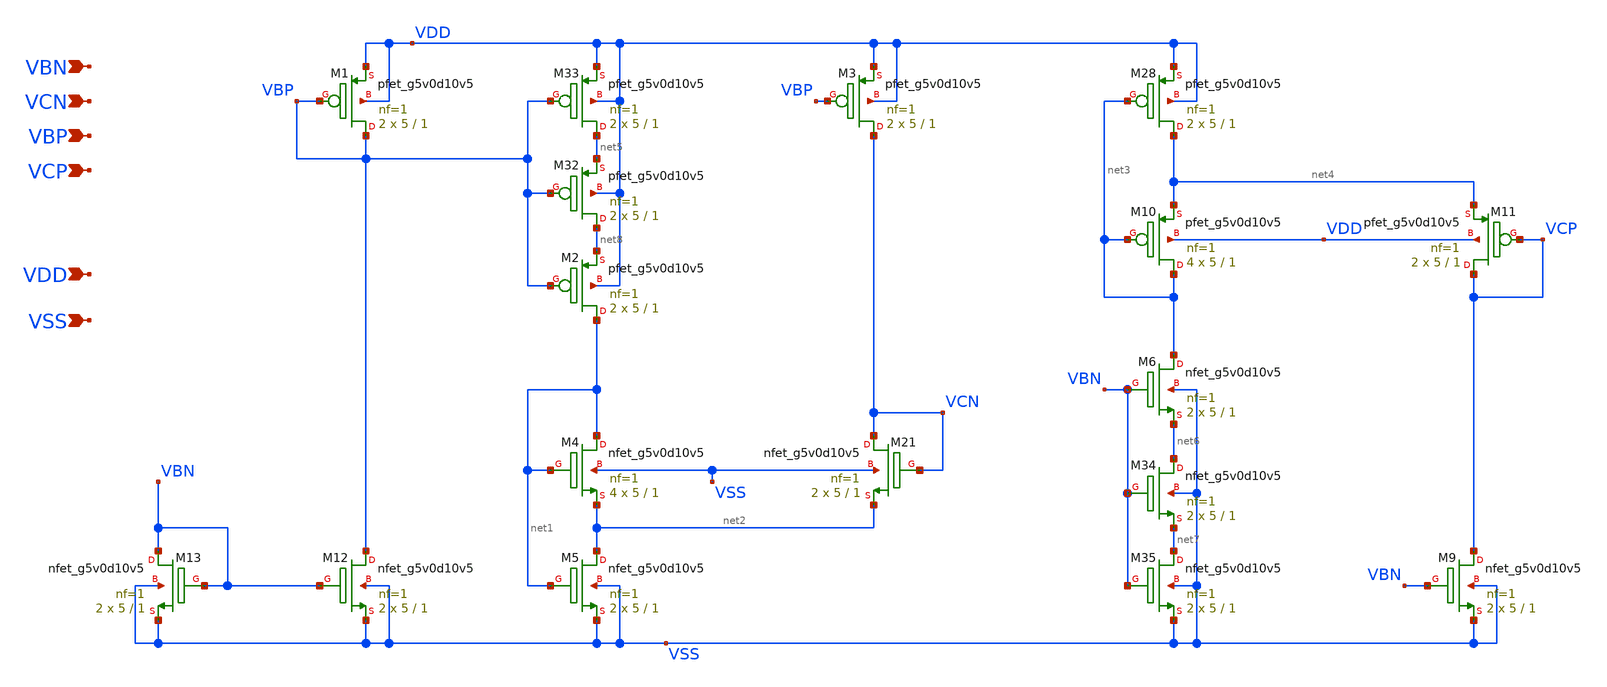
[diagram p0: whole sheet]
** sch_path: design/bias-circuit/cascode_bias.sch
**.subckt cascode_bias VCN VBP VCP VDD VSS VBN
*.ipin VCN
*.ipin VBP
*.ipin VCP
*.ipin VDD
*.ipin VSS
*.ipin VBN
XM1 VBP VBP VDD VDD sky130_fd_pr__pfet_g5v0d10v5 L=1 W=5 nf=1 ad='int((nf+1)/2) * W/nf * 0.29' as='int((nf+2)/2) * W/nf * 0.29'
+ pd='2*int((nf+1)/2) * (W/nf + 0.29)' ps='2*int((nf+2)/2) * (W/nf + 0.29)' nrd='0.29 / W' nrs='0.29 / W'
+ sa=0 sb=0 sd=0 mult=2 m=2
XM2 net1 VBP net8 VDD sky130_fd_pr__pfet_g5v0d10v5 L=1 W=5 nf=1 ad='int((nf+1)/2) * W/nf * 0.29' as='int((nf+2)/2) * W/nf * 0.29'
+ pd='2*int((nf+1)/2) * (W/nf + 0.29)' ps='2*int((nf+2)/2) * (W/nf + 0.29)' nrd='0.29 / W' nrs='0.29 / W'
+ sa=0 sb=0 sd=0 mult=2 m=2
XM3 VCN VBP VDD VDD sky130_fd_pr__pfet_g5v0d10v5 L=1 W=5 nf=1 ad='int((nf+1)/2) * W/nf * 0.29' as='int((nf+2)/2) * W/nf * 0.29'
+ pd='2*int((nf+1)/2) * (W/nf + 0.29)' ps='2*int((nf+2)/2) * (W/nf + 0.29)' nrd='0.29 / W' nrs='0.29 / W'
+ sa=0 sb=0 sd=0 mult=2 m=2
XM4 net1 net1 net2 VSS sky130_fd_pr__nfet_g5v0d10v5 L=1 W=5 nf=1 ad='int((nf+1)/2) * W/nf * 0.29' as='int((nf+2)/2) * W/nf * 0.29'
+ pd='2*int((nf+1)/2) * (W/nf + 0.29)' ps='2*int((nf+2)/2) * (W/nf + 0.29)' nrd='0.29 / W' nrs='0.29 / W'
+ sa=0 sb=0 sd=0 mult=4 m=4
XM5 net2 net1 VSS VSS sky130_fd_pr__nfet_g5v0d10v5 L=1 W=5 nf=1 ad='int((nf+1)/2) * W/nf * 0.29' as='int((nf+2)/2) * W/nf * 0.29'
+ pd='2*int((nf+1)/2) * (W/nf + 0.29)' ps='2*int((nf+2)/2) * (W/nf + 0.29)' nrd='0.29 / W' nrs='0.29 / W'
+ sa=0 sb=0 sd=0 mult=2 m=2
XM21 VCN VCN net2 VSS sky130_fd_pr__nfet_g5v0d10v5 L=1 W=5 nf=1 ad='int((nf+1)/2) * W/nf * 0.29' as='int((nf+2)/2) * W/nf * 0.29'
+ pd='2*int((nf+1)/2) * (W/nf + 0.29)' ps='2*int((nf+2)/2) * (W/nf + 0.29)' nrd='0.29 / W' nrs='0.29 / W'
+ sa=0 sb=0 sd=0 mult=2 m=2
XM6 net3 VBN net6 VSS sky130_fd_pr__nfet_g5v0d10v5 L=1 W=5 nf=1 ad='int((nf+1)/2) * W/nf * 0.29' as='int((nf+2)/2) * W/nf * 0.29'
+ pd='2*int((nf+1)/2) * (W/nf + 0.29)' ps='2*int((nf+2)/2) * (W/nf + 0.29)' nrd='0.29 / W' nrs='0.29 / W'
+ sa=0 sb=0 sd=0 mult=2 m=2
XM9 VCP VBN VSS VSS sky130_fd_pr__nfet_g5v0d10v5 L=1 W=5 nf=1 ad='int((nf+1)/2) * W/nf * 0.29' as='int((nf+2)/2) * W/nf * 0.29'
+ pd='2*int((nf+1)/2) * (W/nf + 0.29)' ps='2*int((nf+2)/2) * (W/nf + 0.29)' nrd='0.29 / W' nrs='0.29 / W'
+ sa=0 sb=0 sd=0 mult=2 m=2
XM10 net3 net3 net4 VDD sky130_fd_pr__pfet_g5v0d10v5 L=1 W=5 nf=1 ad='int((nf+1)/2) * W/nf * 0.29' as='int((nf+2)/2) * W/nf * 0.29'
+ pd='2*int((nf+1)/2) * (W/nf + 0.29)' ps='2*int((nf+2)/2) * (W/nf + 0.29)' nrd='0.29 / W' nrs='0.29 / W'
+ sa=0 sb=0 sd=0 mult=4 m=4
XM11 VCP VCP net4 VDD sky130_fd_pr__pfet_g5v0d10v5 L=1 W=5 nf=1 ad='int((nf+1)/2) * W/nf * 0.29' as='int((nf+2)/2) * W/nf * 0.29'
+ pd='2*int((nf+1)/2) * (W/nf + 0.29)' ps='2*int((nf+2)/2) * (W/nf + 0.29)' nrd='0.29 / W' nrs='0.29 / W'
+ sa=0 sb=0 sd=0 mult=2 m=2
XM28 net4 net3 VDD VDD sky130_fd_pr__pfet_g5v0d10v5 L=1 W=5 nf=1 ad='int((nf+1)/2) * W/nf * 0.29' as='int((nf+2)/2) * W/nf * 0.29'
+ pd='2*int((nf+1)/2) * (W/nf + 0.29)' ps='2*int((nf+2)/2) * (W/nf + 0.29)' nrd='0.29 / W' nrs='0.29 / W'
+ sa=0 sb=0 sd=0 mult=2 m=2
XM12 VBP VBN VSS VSS sky130_fd_pr__nfet_g5v0d10v5 L=1 W=5 nf=1 ad='int((nf+1)/2) * W/nf * 0.29' as='int((nf+2)/2) * W/nf * 0.29'
+ pd='2*int((nf+1)/2) * (W/nf + 0.29)' ps='2*int((nf+2)/2) * (W/nf + 0.29)' nrd='0.29 / W' nrs='0.29 / W'
+ sa=0 sb=0 sd=0 mult=2 m=2
XM32 net8 VBP net5 VDD sky130_fd_pr__pfet_g5v0d10v5 L=1 W=5 nf=1 ad='int((nf+1)/2) * W/nf * 0.29' as='int((nf+2)/2) * W/nf * 0.29'
+ pd='2*int((nf+1)/2) * (W/nf + 0.29)' ps='2*int((nf+2)/2) * (W/nf + 0.29)' nrd='0.29 / W' nrs='0.29 / W'
+ sa=0 sb=0 sd=0 mult=2 m=2
XM33 net5 VBP VDD VDD sky130_fd_pr__pfet_g5v0d10v5 L=1 W=5 nf=1 ad='int((nf+1)/2) * W/nf * 0.29' as='int((nf+2)/2) * W/nf * 0.29'
+ pd='2*int((nf+1)/2) * (W/nf + 0.29)' ps='2*int((nf+2)/2) * (W/nf + 0.29)' nrd='0.29 / W' nrs='0.29 / W'
+ sa=0 sb=0 sd=0 mult=2 m=2
XM34 net6 VBN net7 VSS sky130_fd_pr__nfet_g5v0d10v5 L=1 W=5 nf=1 ad='int((nf+1)/2) * W/nf * 0.29' as='int((nf+2)/2) * W/nf * 0.29'
+ pd='2*int((nf+1)/2) * (W/nf + 0.29)' ps='2*int((nf+2)/2) * (W/nf + 0.29)' nrd='0.29 / W' nrs='0.29 / W'
+ sa=0 sb=0 sd=0 mult=2 m=2
XM35 net7 VBN VSS VSS sky130_fd_pr__nfet_g5v0d10v5 L=1 W=5 nf=1 ad='int((nf+1)/2) * W/nf * 0.29' as='int((nf+2)/2) * W/nf * 0.29'
+ pd='2*int((nf+1)/2) * (W/nf + 0.29)' ps='2*int((nf+2)/2) * (W/nf + 0.29)' nrd='0.29 / W' nrs='0.29 / W'
+ sa=0 sb=0 sd=0 mult=2 m=2
XM13 VBN VBN VSS VSS sky130_fd_pr__nfet_g5v0d10v5 L=1 W=5 nf=1 ad='int((nf+1)/2) * W/nf * 0.29' as='int((nf+2)/2) * W/nf * 0.29'
+ pd='2*int((nf+1)/2) * (W/nf + 0.29)' ps='2*int((nf+2)/2) * (W/nf + 0.29)' nrd='0.29 / W' nrs='0.29 / W'
+ sa=0 sb=0 sd=0 mult=2 m=2
**.ends
.end
